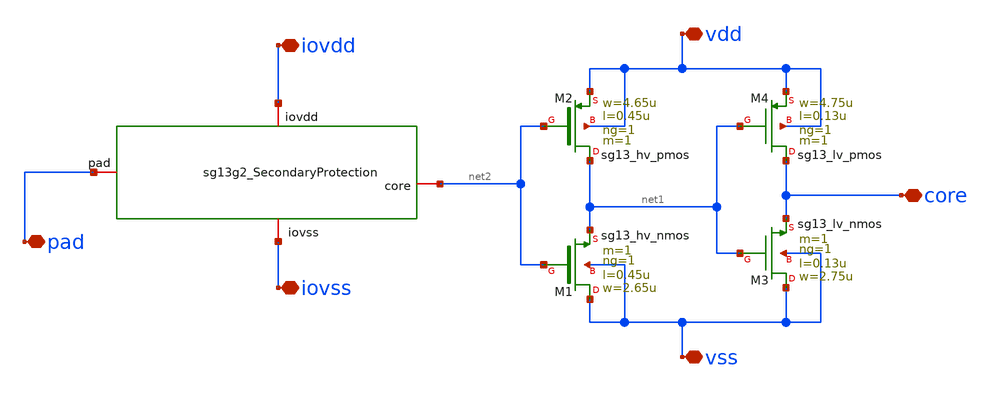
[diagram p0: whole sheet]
** sch_path: ihp-sg13g2/libs.ref/sg13g2_io/xschem/sg13g2_LevelDown.sch
**.subckt sg13g2_LevelDown vdd vss iovdd iovss pad core
*.iopin vdd
*.iopin vss
*.iopin iovdd
*.iopin iovss
*.iopin pad
*.iopin core
XM1 vss net2 net1 vss sg13_hv_nmos w=2.65u l=0.45u ng=1 m=1 mm_ok=1
XM2 net1 net2 vdd vdd sg13_hv_pmos w=4.65u l=0.45u ng=1 m=1 mm_ok=1
XM3 vss net1 core vss sg13_lv_nmos w=2.75u l=0.13u ng=1 m=1 mm_ok=1
XM4 core net1 vdd vdd sg13_lv_pmos w=4.75u l=0.13u ng=1 m=1 mm_ok=1
**.ends
.end
